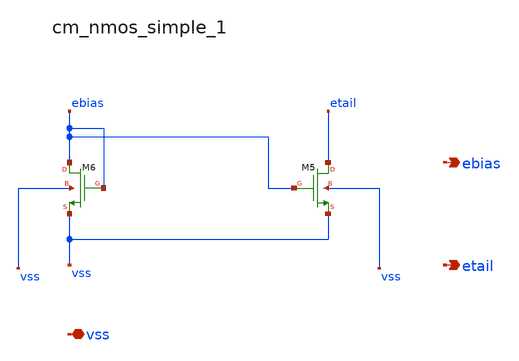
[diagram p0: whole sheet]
** sch_path: analog-db/raw/ldo_007_pmos/hier/blocks/cm_nmos_simple_1.sch
**.subckt cm_nmos_simple_1 vss ebias etail
*.iopin vss
*.opin ebias
*.opin etail
XM5 etail ebias vss vss sg13_lv_nmos w=x_dut_xm5_w l=x_dut_xm5_l ng=1 m=1
XM6 ebias ebias vss vss sg13_lv_nmos w=x_dut_xm6_w l=x_dut_xm6_l ng=1 m=1
**.ends
.end
